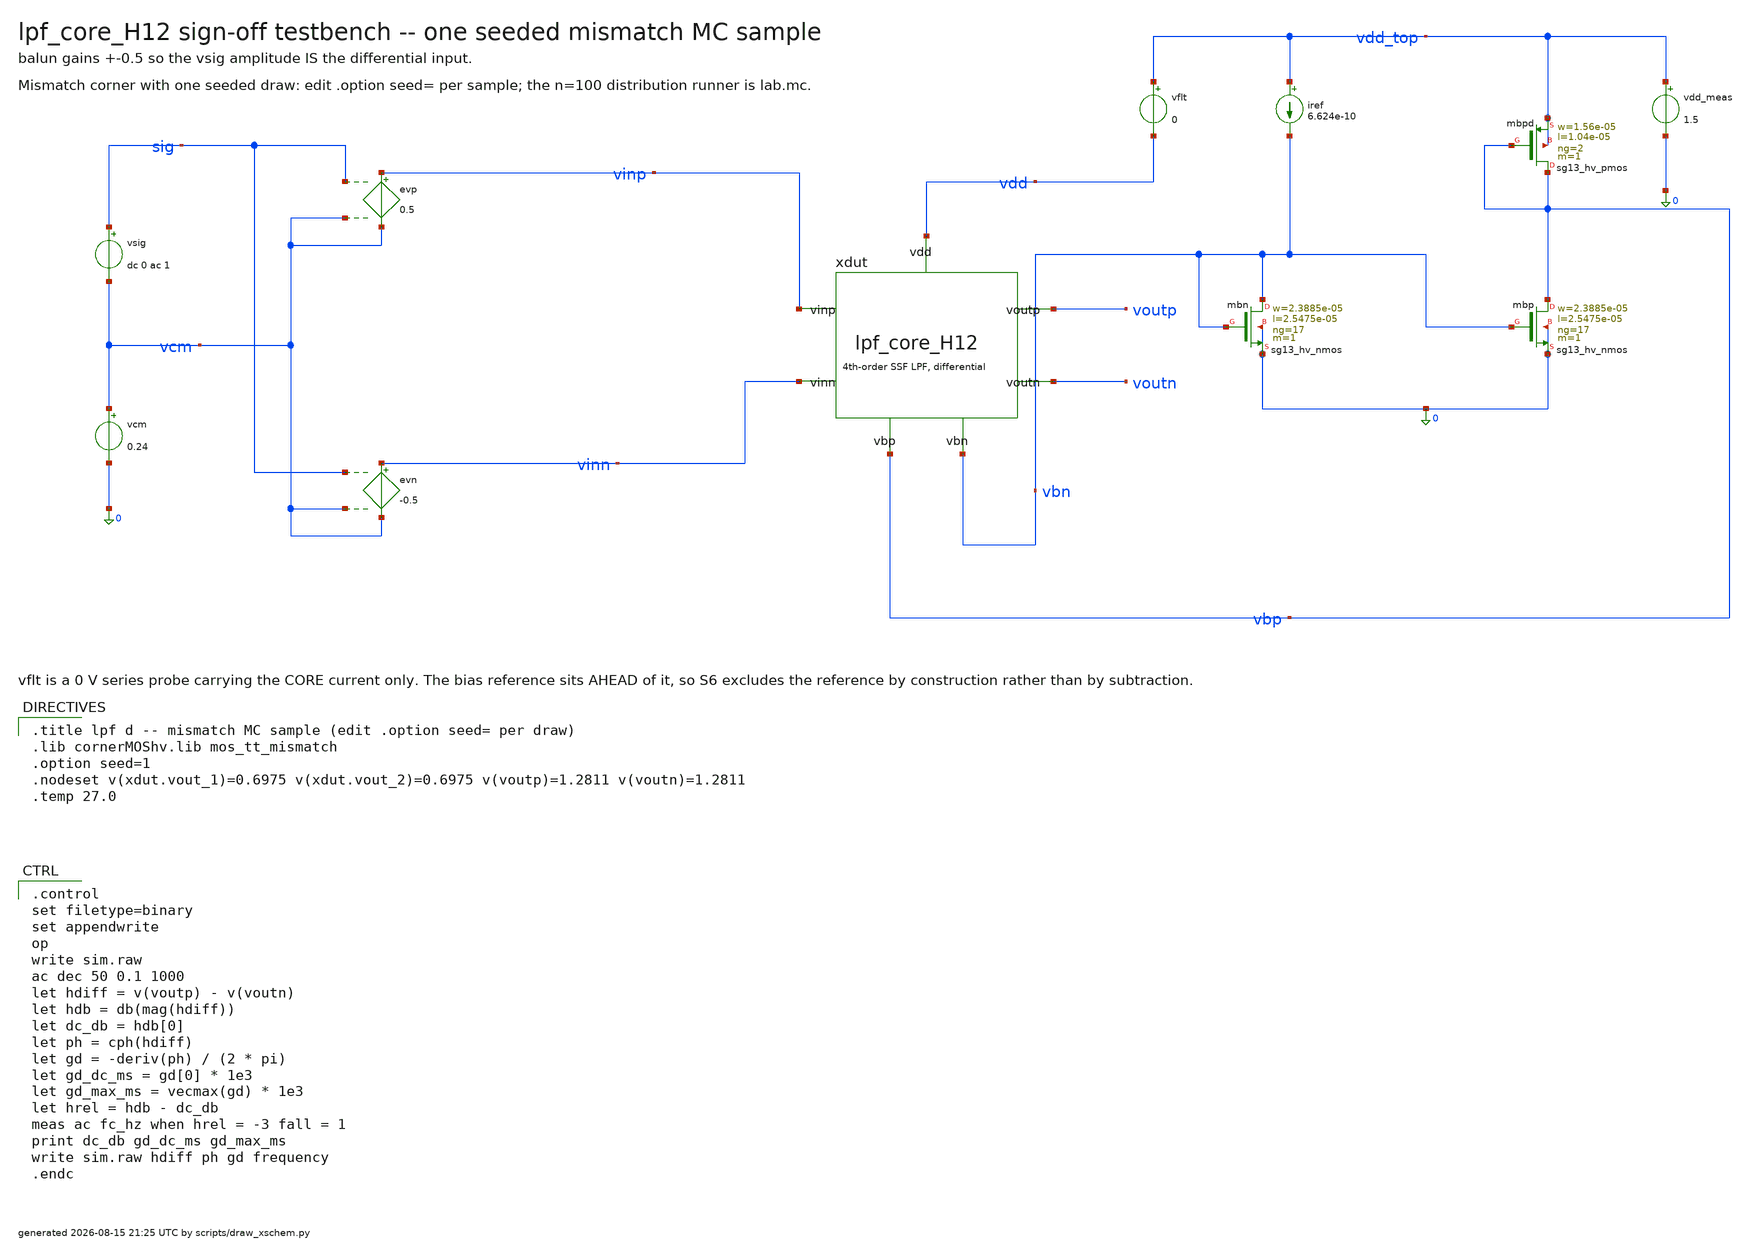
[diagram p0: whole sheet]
** sch_path: signoff/post-pvt/H12-robust/lpf_tb_H12_mc.sch
**.subckt lpf_tb_H12_mc
vsig sig vcm dc 0 ac 1
vcm vcm 0 0.24
evp vinp vcm sig vcm 0.5
evn vinn vcm sig vcm -0.5
xdut vinp vinn voutp voutn vbn vbp vdd lpf_core_H12
vflt vdd_top vdd 0
vdd_meas vdd_top 0 1.5
iref vdd_top vbn 6.624e-10
Xmbn vbn vbn 0 0 sg13_hv_nmos w=2.3885e-05 l=2.5475e-05 ng=17 m=1 mm_ok=1
Xmbp vbp vbn 0 0 sg13_hv_nmos w=2.3885e-05 l=2.5475e-05 ng=17 m=1 mm_ok=1
Xmbpd vbp vbp vdd_top vdd_top sg13_hv_pmos w=1.56e-05 l=1.04e-05 ng=2 m=1 mm_ok=1
**** begin user architecture code

.title lpf d -- mismatch MC sample (edit .option seed= per draw)
.lib cornerMOShv.lib mos_tt_mismatch
.option seed=1
.nodeset v(xdut.vout_1)=0.6975 v(xdut.vout_2)=0.6975 v(voutp)=1.2811 v(voutn)=1.2811
.temp 27.0


.control
set filetype=binary
set appendwrite
op
write sim.raw
ac dec 50 0.1 1000
let hdiff = v(voutp) - v(voutn)
let hdb = db(mag(hdiff))
let dc_db = hdb[0]
let ph = cph(hdiff)
let gd = -deriv(ph) / (2 * pi)
let gd_dc_ms = gd[0] * 1e3
let gd_max_ms = vecmax(gd) * 1e3
let hrel = hdb - dc_db
meas ac fc_hz when hrel = -3 fall = 1
print dc_db gd_dc_ms gd_max_ms
write sim.raw hdiff ph gd frequency
.endc

**** end user architecture code
**.ends

* expanding   symbol:  lpf_core_H12.sym # of pins=7
** sym_path: signoff/post-pvt/H12-robust/lpf_core_H12.sym
** sch_path: signoff/post-pvt/H12-robust/lpf_core_H12.sch
.subckt lpf_core_H12 vinp vinn voutp voutn vbn vbp vdd
*.ipin vinp
*.ipin vinn
*.opin voutp
*.opin voutn
*.ipin vdd
*.ipin vbn
*.ipin vbp
Xm2 net2 vinp vout_1 vout_1 sg13_hv_pmos w=1.56e-05 l=1.04e-05 ng=2 m=1 mm_ok=1
Xm5 net3 vinn vout_2 vout_2 sg13_hv_pmos w=1.56e-05 l=1.04e-05 ng=2 m=1 mm_ok=1
Xm4 vout_1 net2 0 0 sg13_hv_nmos w=1.5e-06 l=4.5e-05 ng=1 m=1 mm_ok=1
Xm8 vout_2 net3 0 0 sg13_hv_nmos w=1.5e-06 l=4.5e-05 ng=1 m=1 mm_ok=1
Xm9 net2 vbn 0 0 sg13_hv_nmos w=2.3885e-05 l=2.5475e-05 ng=17 m=1 mm_ok=1
Xm10 net3 vbn 0 0 sg13_hv_nmos w=2.3885e-05 l=2.5475e-05 ng=17 m=1 mm_ok=1
Xmst vout_1 vbr net4 net4 sg13_hv_pmos w=4.86e-06 l=3.276e-05 ng=1 m=1 mm_ok=1
Xmstn vout_2 vbr net1 net1 sg13_hv_pmos w=4.86e-06 l=3.276e-05 ng=1 m=1 mm_ok=1
Xm0 net4 vout_1 voutp voutp sg13_hv_pmos w=4e-06 l=1.5e-05 ng=1 m=1 mm_ok=1
Xm1 net1 vout_2 voutn voutn sg13_hv_pmos w=4e-06 l=1.5e-05 ng=1 m=1 mm_ok=1
Xm14 voutp net4 vdd vdd sg13_hv_pmos w=1.202e-05 l=3.1115e-05 ng=2 m=1 mm_ok=1
Xm15 voutn net1 vdd vdd sg13_hv_pmos w=1.202e-05 l=3.1115e-05 ng=2 m=1 mm_ok=1
Xr1 rep_x rep_x vdd vdd sg13_hv_pmos w=1.202e-05 l=3.1115e-05 ng=2 m=1 mm_ok=1
Xr2 vbr vbr rep_x rep_x sg13_hv_pmos w=4.86e-06 l=3.276e-05 ng=1 m=1 mm_ok=1
Xr3 vbr vbn 0 0 sg13_hv_nmos w=2.3885e-05 l=2.5475e-05 ng=17 m=4 mm_ok=1
c13 net2 vout_1 5.00659e-12 m=1
c17 net3 vout_2 5.00659e-12 m=1
c19 vout_2 vout_1 2.89483e-11 m=1
c1 voutp net4 6.0258e-11 m=1
c10 voutn net1 6.0258e-11 m=1
c12 voutn voutp 2.39864e-11 m=1
.ends

.end
